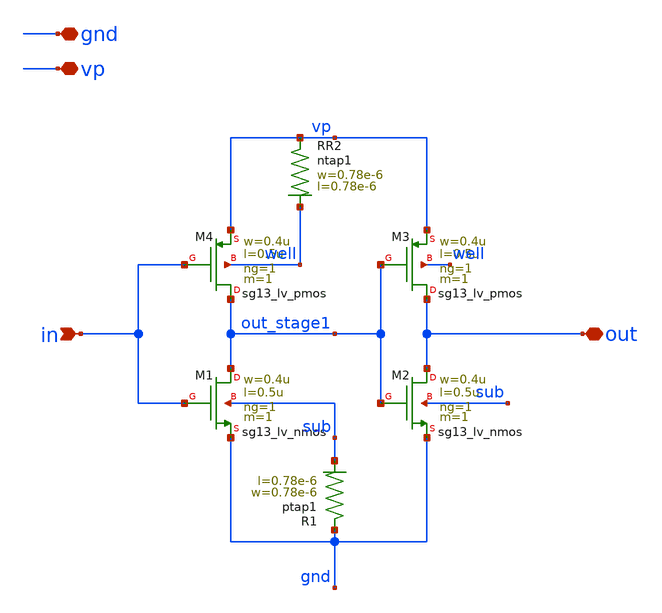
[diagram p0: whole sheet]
** sch_path: schematics/PFD/PFD_buffor.sch
**.subckt PFD_buffor gnd vp in out
*.iopin gnd
*.iopin vp
*.ipin in
*.iopin out
XM1 out_stage1 in gnd sub sg13_lv_nmos w=0.4u l=0.5u ng=1 m=1 mm_ok=1
XM4 out_stage1 in vp well sg13_lv_pmos w=0.4u l=0.5u ng=1 m=1 mm_ok=1
XM2 out out_stage1 gnd sub sg13_lv_nmos w=0.4u l=0.5u ng=1 m=1 mm_ok=1
XM3 out out_stage1 vp well sg13_lv_pmos w=0.4u l=0.5u ng=1 m=1 mm_ok=1
XR1 gnd sub ptap1 R=262.8 w=0.78e-6 l=0.78e-6
XR2 vp well ntap1 R=262.8 w=0.78e-6 l=0.78e-6
**.ends
.end
